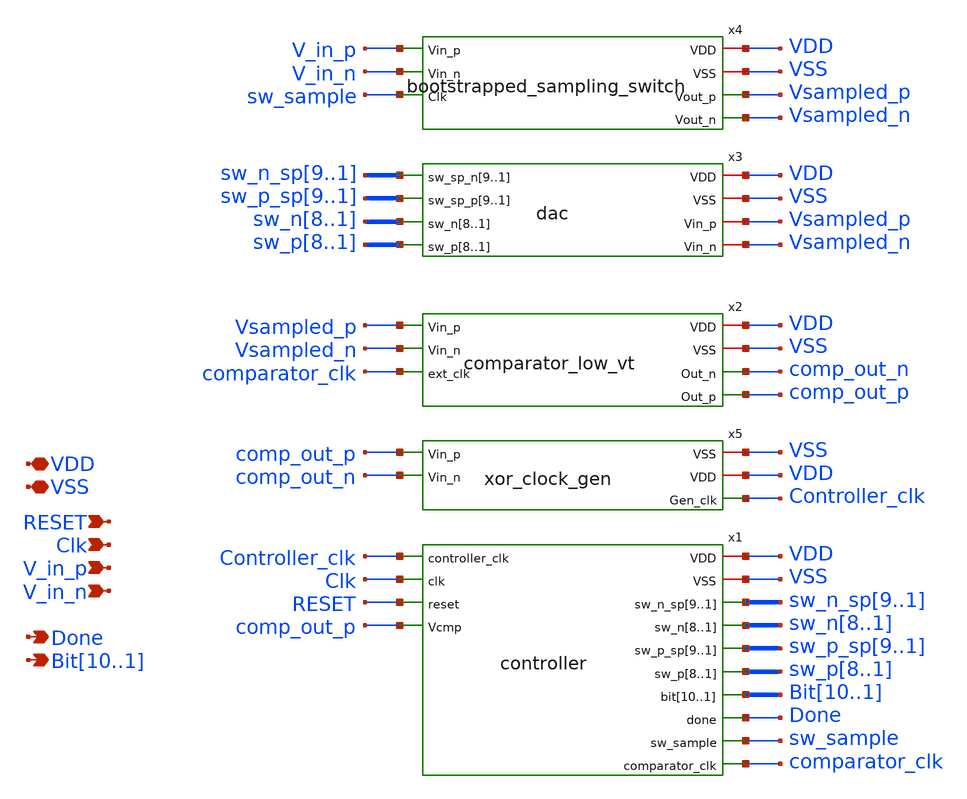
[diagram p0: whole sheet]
** sch_path: xschem/src/sar_adc/sar_adc_low_vt.sch
**.subckt sar_adc_low_vt VDD V_in_p Done VSS V_in_n Clk
*+ Bit10,Bit9,Bit8,Bit7,Bit6,Bit5,Bit4,Bit3,Bit2,Bit1 RESET
*.iopin VDD
*.ipin V_in_p
*.opin Done
*.iopin VSS
*.ipin V_in_n
*.ipin Clk
*.opin Bit10,Bit9,Bit8,Bit7,Bit6,Bit5,Bit4,Bit3,Bit2,Bit1
*.ipin RESET
x1 VDD Controller_clk VSS sw_n_sp9 sw_n_sp8 sw_n_sp7 sw_n_sp6 sw_n_sp5 sw_n_sp4 sw_n_sp3 sw_n_sp2
+ sw_n_sp1 Clk sw_n8 sw_n7 sw_n6 sw_n5 sw_n4 sw_n3 sw_n2 sw_n1 RESET comp_out_p sw_p_sp9 sw_p_sp8 sw_p_sp7
+ sw_p_sp6 sw_p_sp5 sw_p_sp4 sw_p_sp3 sw_p_sp2 sw_p_sp1 sw_p8 sw_p7 sw_p6 sw_p5 sw_p4 sw_p3 sw_p2 sw_p1 Bit10
+ Bit9 Bit8 Bit7 Bit6 Bit5 Bit4 Bit3 Bit2 Bit1 Done sw_sample comparator_clk controller
x3 sw_n_sp9 sw_n_sp8 sw_n_sp7 sw_n_sp6 sw_n_sp5 sw_n_sp4 sw_n_sp3 sw_n_sp2 sw_n_sp1 VDD sw_p_sp9
+ sw_p_sp8 sw_p_sp7 sw_p_sp6 sw_p_sp5 sw_p_sp4 sw_p_sp3 sw_p_sp2 sw_p_sp1 VSS sw_n8 sw_n7 sw_n6 sw_n5 sw_n4
+ sw_n3 sw_n2 sw_n1 Vsampled_p sw_p8 sw_p7 sw_p6 sw_p5 sw_p4 sw_p3 sw_p2 sw_p1 Vsampled_n dac
x4 VDD V_in_p VSS V_in_n sw_sample Vsampled_p Vsampled_n bootstrapped_sampling_switch
x5 VSS comp_out_p VDD comp_out_n Controller_clk xor_clock_gen
x2 VDD VSS Vsampled_p comp_out_n Vsampled_n comparator_clk comp_out_p comparator_low_vt
**.ends
.end
